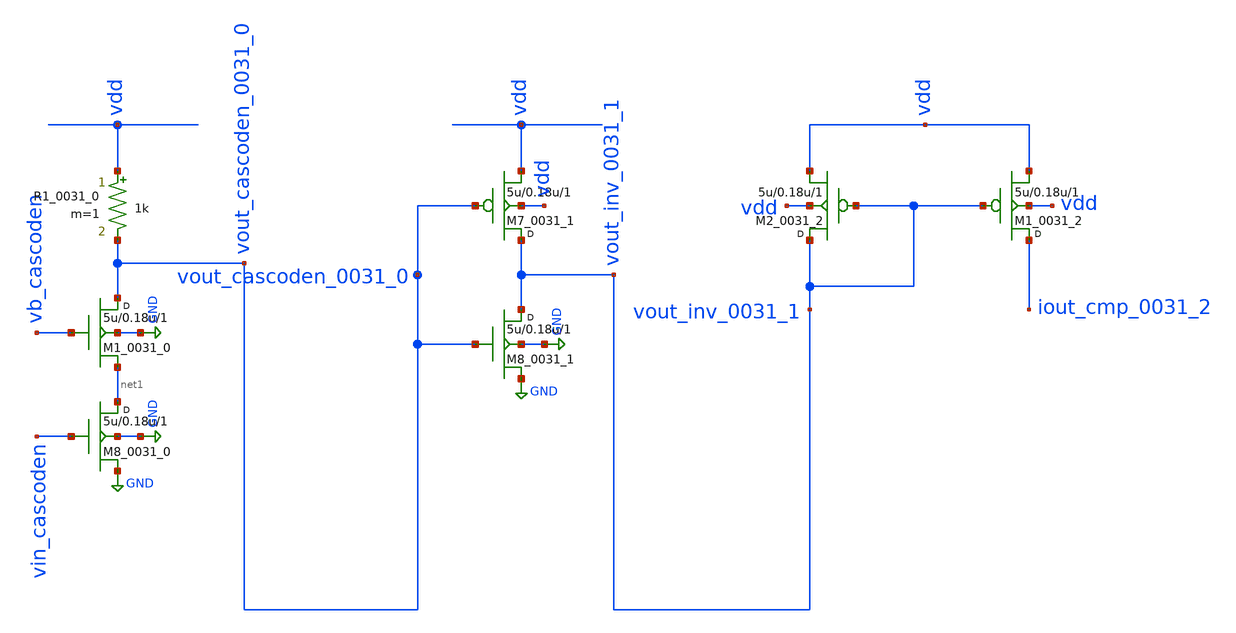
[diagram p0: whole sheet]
** sch_path: synthetic/generated/0031_generated.sch
**.subckt 0031_generated
M8_0031_0 net1 vin_cascoden GND GND nmos w=5u l=0.18u m=1
M1_0031_0 vout_cascoden_0031_0 vb_cascoden net1 GND nmos w=5u l=0.18u m=1
R1_0031_0 vdd vout_cascoden_0031_0 1k m=1
M7_0031_1 vout_inv_0031_1 vout_cascoden_0031_0 vdd vdd pmos w=5u l=0.18u m=1
M8_0031_1 vout_inv_0031_1 vout_cascoden_0031_0 GND GND nmos w=5u l=0.18u m=1
M1_0031_2 iout_cmp_0031_2 vout_inv_0031_1 vdd vdd pmos w=5u l=0.18u m=1
M2_0031_2 vout_inv_0031_1 vout_inv_0031_1 vdd vdd pmos w=5u l=0.18u m=1
**.ends
.GLOBAL GND
.end
